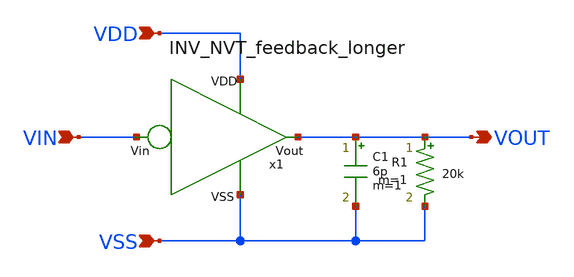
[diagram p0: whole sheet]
** sch_path: design/THESIS_EXP_RO_INVERTER_SKY130A/TB_Cin_NVT_LL.sch
**.subckt TB_Cin_NVT_LL VOUT VIN VSS VDD
*.opin VOUT
*.ipin VIN
*.ipin VSS
*.ipin VDD
C1 VOUT VSS 6p m=1
R1 VOUT VSS 20k m=1
x1 VDD VSS VOUT VIN INV_NVT_feedback_longer
**.ends
.end
